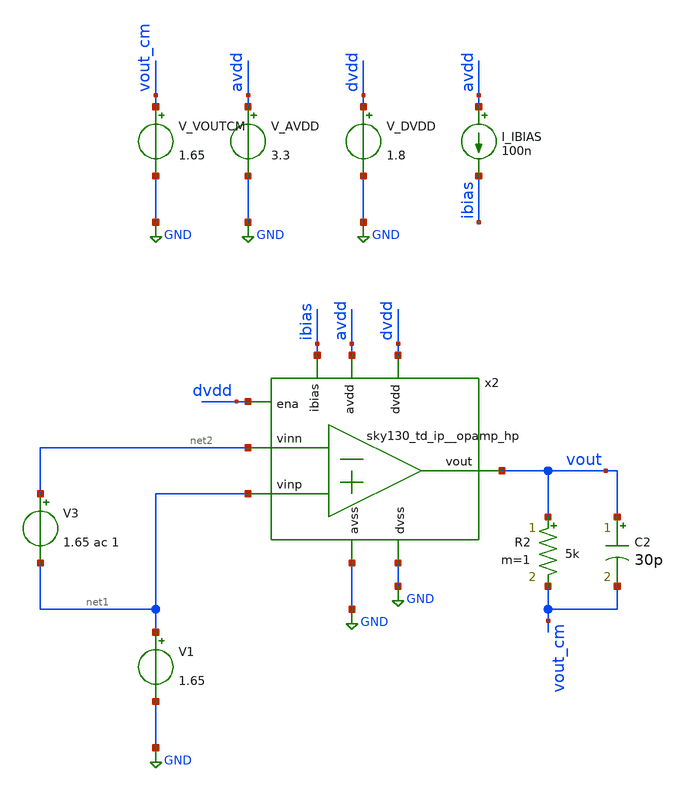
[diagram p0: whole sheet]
** sch_path: xschem/noise.sch
**.subckt noise
V_AVDD avdd GND 3.3
.save i(v_avdd)
V_DVDD dvdd GND 1.8
.save i(v_dvdd)
I_IBIAS avdd ibias 100n
V_VOUTCM vout_cm GND 1.65
.save i(v_voutcm)
x2 avdd vout ibias net2 net1 GND dvdd GND dvdd sky130_td_ip__opamp_hp
R2 vout vout_cm 5k m=1
C2 vout vout_cm 30p m=1
V3 net2 net1 1.65 ac 1
V1 net1 GND 1.65
**** begin user architecture code


.save all


* .noise v(vout) V3 dec 100 100 90MEG

.control
save all
set sqrnoise
noise V(vout) V3 dec 100 100 1e6
print inoise_total onoise_total

setplot noise1
let vn = sqrt(onoise_spectrum[0])
echo vn = $&vn
plot inoise_spectrum

.endc




.lib /usr/local/share/pdk/sky130A/libs.tech/combined/sky130.lib.spice tt


**** end user architecture code
**.ends
.GLOBAL GND
.end
